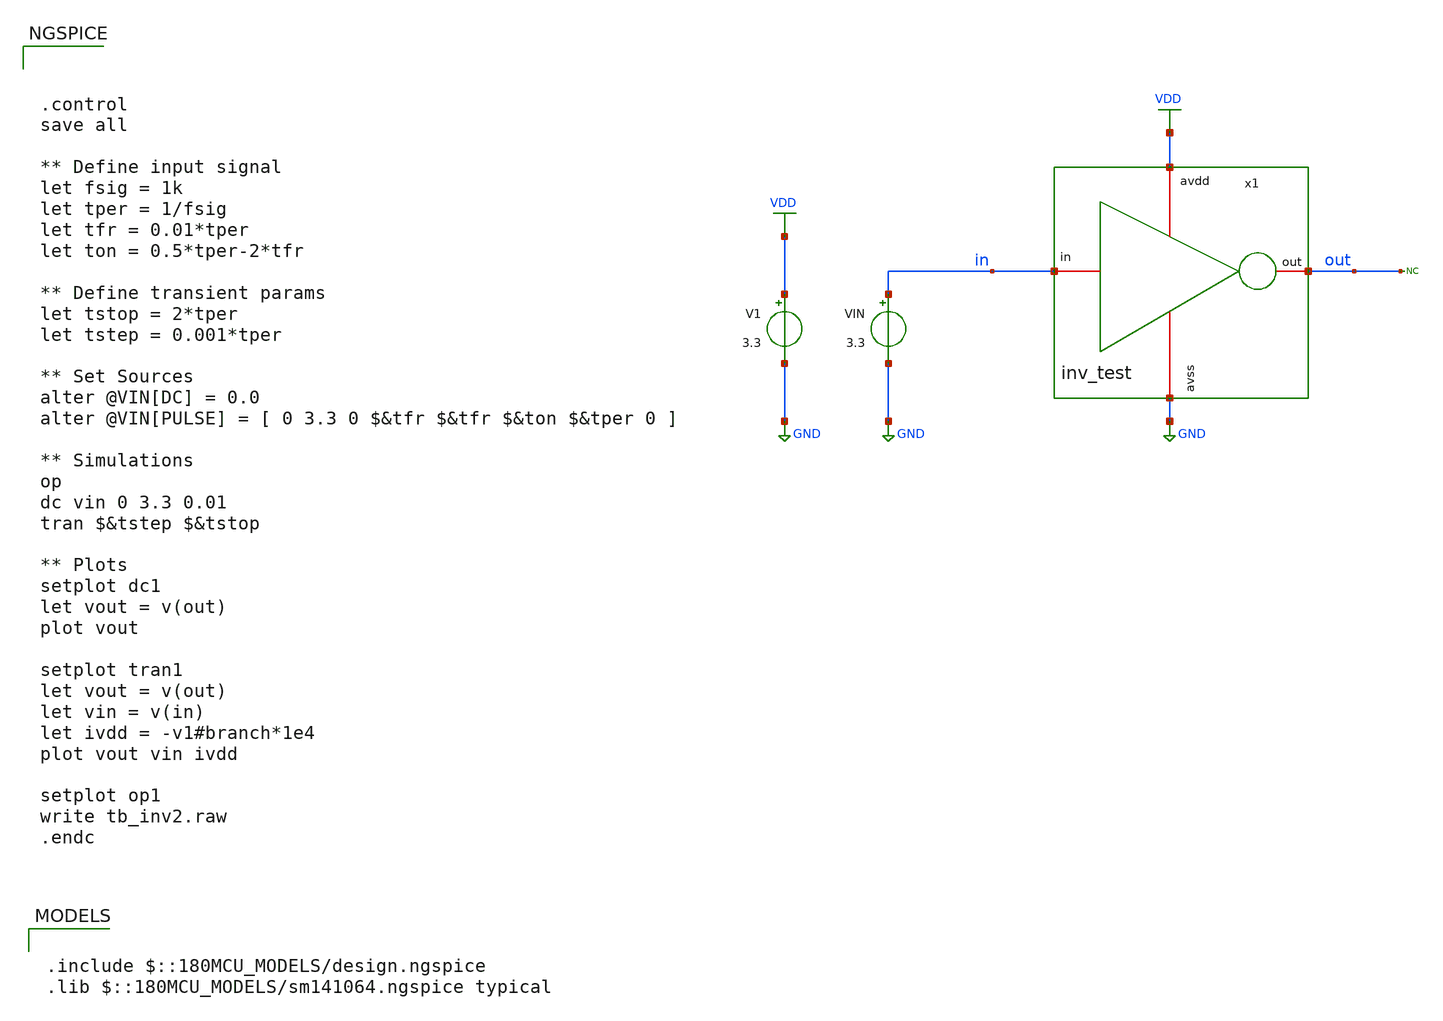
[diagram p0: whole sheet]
** sch_path: designs/libs/wk_kadam/tb_inv2.sch
**.subckt tb_inv2
x1 VDD in out GND inv_test
V1 VDD GND 3.3
VIN in GND 3.3
* noconn out
**** begin user architecture code



.control
save all

** Define input signal
let fsig = 1k
let tper = 1/fsig
let tfr = 0.01*tper
let ton = 0.5*tper-2*tfr

** Define transient params
let tstop = 2*tper
let tstep = 0.001*tper

** Set Sources
alter @VIN[DC] = 0.0
alter @VIN[PULSE] = [ 0 3.3 0 $&tfr $&tfr $&ton $&tper 0 ]

** Simulations
op
dc vin 0 3.3 0.01
tran $&tstep $&tstop

** Plots
setplot dc1
let vout = v(out)
plot vout

setplot tran1
let vout = v(out)
let vin = v(in)
let ivdd = -v1#branch*1e4
plot vout vin ivdd

setplot op1
write tb_inv2.raw
.endc



.include $::180MCU_MODELS/design.ngspice
.lib $::180MCU_MODELS/sm141064.ngspice typical

**** end user architecture code
**.ends

* expanding   symbol:  libs/wk_kadam/inv_test.sym # of pins=4
** sym_path: designs/libs/wk_kadam/inv_test.sym
** sch_path: designs/libs/wk_kadam/inv_test.sch
.subckt inv_test avdd in out avss
*.iopin avdd
*.iopin avss
*.iopin in
*.iopin out
XM3 out in avss avss nfet_03v3 L=0.28u W=1.0u nf=1 ad='int((nf+1)/2) * W/nf * 0.18u' as='int((nf+2)/2) * W/nf * 0.18u'
+ pd='2*int((nf+1)/2) * (W/nf + 0.18u)' ps='2*int((nf+2)/2) * (W/nf + 0.18u)' nrd='0.18u / W' nrs='0.18u / W'
+ sa=0 sb=0 sd=0 m=1
XM4 out in avdd avdd pfet_03v3 L=0.28u W=2.0u nf=1 ad='int((nf+1)/2) * W/nf * 0.18u' as='int((nf+2)/2) * W/nf * 0.18u'
+ pd='2*int((nf+1)/2) * (W/nf + 0.18u)' ps='2*int((nf+2)/2) * (W/nf + 0.18u)' nrd='0.18u / W' nrs='0.18u / W'
+ sa=0 sb=0 sd=0 m=1
.ends

.GLOBAL VDD
.GLOBAL GND
.end
